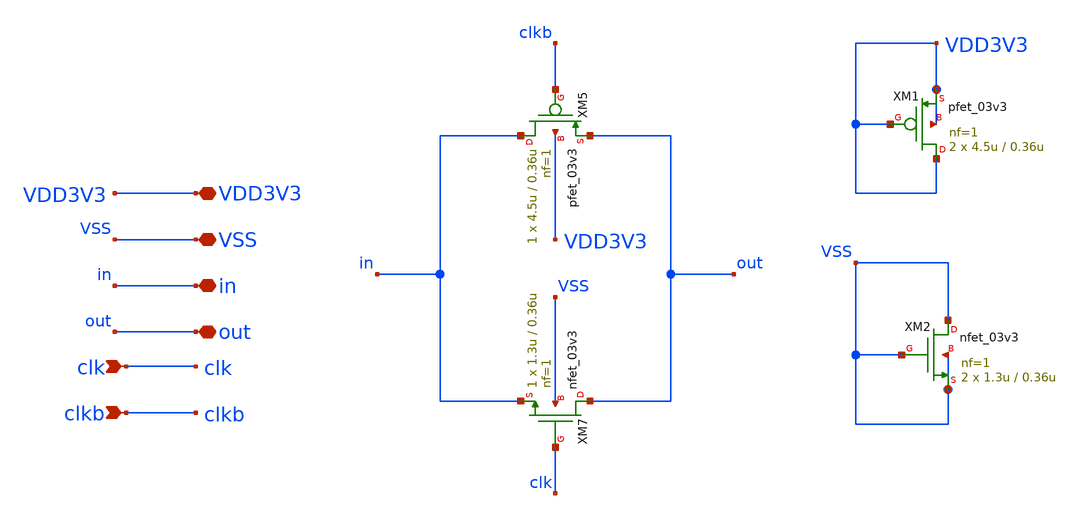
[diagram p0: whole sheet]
** sch_path: designs/libs/core_pga/switch/switch.sch
**.subckt switch VSS VDD3V3 clk clkb in out
*.iopin VSS
*.iopin VDD3V3
*.ipin clk
*.ipin clkb
*.iopin in
*.iopin out
XM5 in clkb out VDD3V3 pfet_03v3 L=0.36u W=4.5u nf=1 ad='int((nf+1)/2) * W/nf * 0.18u' as='int((nf+2)/2) * W/nf * 0.18u'
+ pd='2*int((nf+1)/2) * (W/nf + 0.18u)' ps='2*int((nf+2)/2) * (W/nf + 0.18u)' nrd='0.18u / W' nrs='0.18u / W'
+ sa=0 sb=0 sd=0 m=1
XM7 out clk in VSS nfet_03v3 L=0.36u W=1.3u nf=1 ad='int((nf+1)/2) * W/nf * 0.18u' as='int((nf+2)/2) * W/nf * 0.18u'
+ pd='2*int((nf+1)/2) * (W/nf + 0.18u)' ps='2*int((nf+2)/2) * (W/nf + 0.18u)' nrd='0.18u / W' nrs='0.18u / W'
+ sa=0 sb=0 sd=0 m=1
XM1 VDD3V3 VDD3V3 VDD3V3 VDD3V3 pfet_03v3 L=0.36u W=4.5u nf=1 ad='int((nf+1)/2) * W/nf * 0.18u' as='int((nf+2)/2) * W/nf * 0.18u'
+ pd='2*int((nf+1)/2) * (W/nf + 0.18u)' ps='2*int((nf+2)/2) * (W/nf + 0.18u)' nrd='0.18u / W' nrs='0.18u / W'
+ sa=0 sb=0 sd=0 m=2
XM2 VSS VSS VSS VSS nfet_03v3 L=0.36u W=1.3u nf=1 ad='int((nf+1)/2) * W/nf * 0.18u' as='int((nf+2)/2) * W/nf * 0.18u'
+ pd='2*int((nf+1)/2) * (W/nf + 0.18u)' ps='2*int((nf+2)/2) * (W/nf + 0.18u)' nrd='0.18u / W' nrs='0.18u / W'
+ sa=0 sb=0 sd=0 m=2
**.ends
.end
